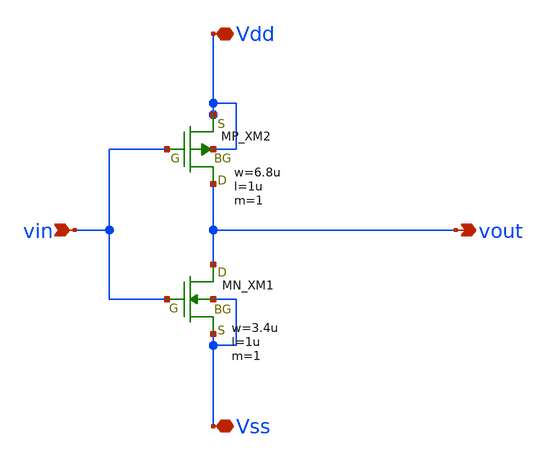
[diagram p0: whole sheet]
** sch_path: inverter.sch
**.subckt inverter vin Vdd Vss vout
*.ipin vin
*.iopin Vdd
*.iopin Vss
*.opin vout
XXM1 vout vin Vss Vss NMOS w=3.4u l=1u nrd=0 nrs=0 m=1
XXM2 vout vin Vdd Vdd PMOS w=6.8u l=1u nrd=0 nrs=0 m=1
**.ends
.end
